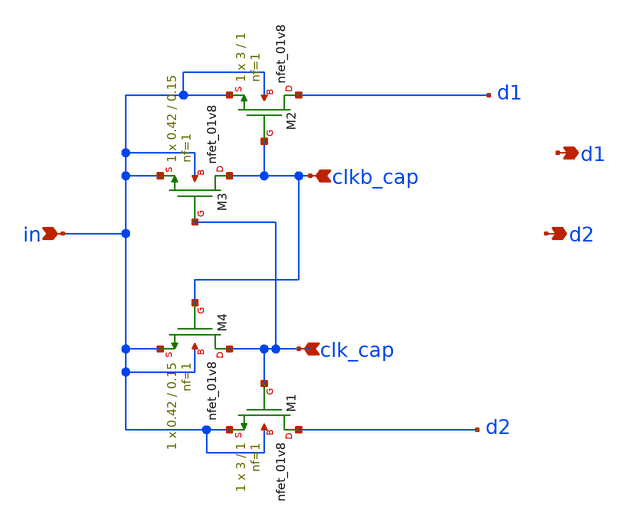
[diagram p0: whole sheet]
** sch_path: xschem/nmos_dnw.sch
**.subckt nmos_dnw in clk_cap d1 d2 clkb_cap
*.ipin in
*.ipin clk_cap
*.opin d1
*.opin d2
*.ipin clkb_cap
XM2 d1 clkb_cap in in sky130_fd_pr__nfet_01v8 L=1 W=3 nf=1 ad='int((nf+1)/2) * W/nf * 0.29' as='int((nf+2)/2) * W/nf * 0.29'
+ pd='2*int((nf+1)/2) * (W/nf + 0.29)' ps='2*int((nf+2)/2) * (W/nf + 0.29)' nrd='0.29 / W' nrs='0.29 / W'
+ sa=0 sb=0 sd=0 mult=1 m=1
XM1 d2 clk_cap in in sky130_fd_pr__nfet_01v8 L=1 W=3 nf=1 ad='int((nf+1)/2) * W/nf * 0.29' as='int((nf+2)/2) * W/nf * 0.29'
+ pd='2*int((nf+1)/2) * (W/nf + 0.29)' ps='2*int((nf+2)/2) * (W/nf + 0.29)' nrd='0.29 / W' nrs='0.29 / W'
+ sa=0 sb=0 sd=0 mult=1 m=1
XM3 clkb_cap clk_cap in in sky130_fd_pr__nfet_01v8 L=0.15 W=0.42 nf=1 ad='int((nf+1)/2) * W/nf * 0.29'
+ as='int((nf+2)/2) * W/nf * 0.29' pd='2*int((nf+1)/2) * (W/nf + 0.29)' ps='2*int((nf+2)/2) * (W/nf + 0.29)'
+ nrd='0.29 / W' nrs='0.29 / W' sa=0 sb=0 sd=0 mult=1 m=1
XM4 clk_cap clkb_cap in in sky130_fd_pr__nfet_01v8 L=0.15 W=0.42 nf=1 ad='int((nf+1)/2) * W/nf * 0.29'
+ as='int((nf+2)/2) * W/nf * 0.29' pd='2*int((nf+1)/2) * (W/nf + 0.29)' ps='2*int((nf+2)/2) * (W/nf + 0.29)'
+ nrd='0.29 / W' nrs='0.29 / W' sa=0 sb=0 sd=0 mult=1 m=1
**.ends
.end
